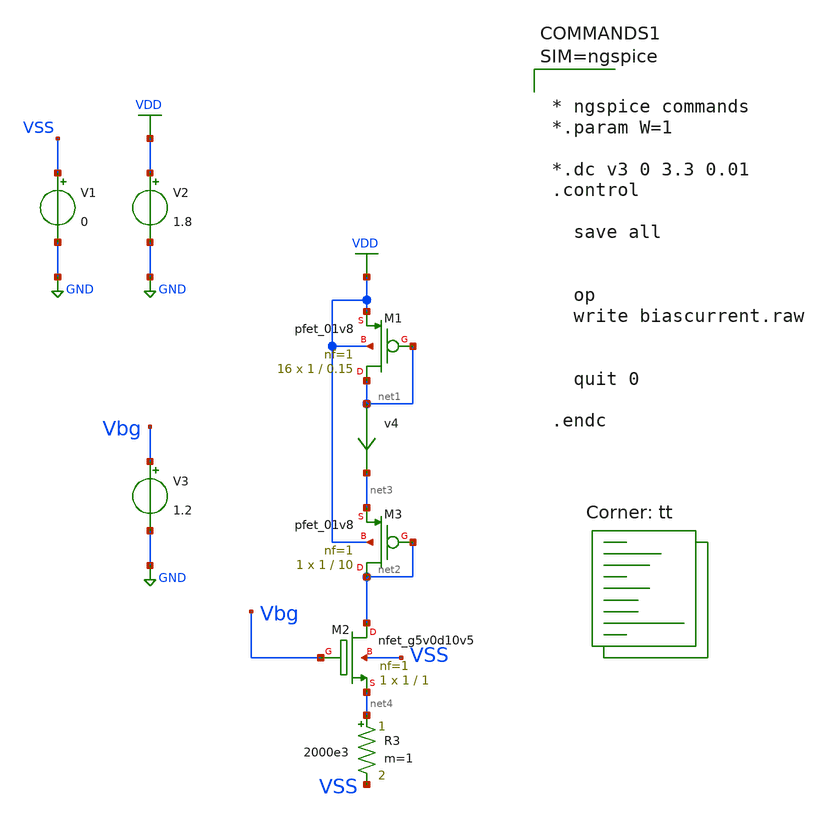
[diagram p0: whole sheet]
** sch_path: xschem/biascurrent.sch
**.subckt biascurrent
v4 net1 net3 0
.save i(v4)
V1 VSS GND 0
V2 VDD GND 1.8
XM1 net1 net1 VDD VDD sky130_fd_pr__pfet_01v8 L=0.15 W=1 nf=1 ad='int((nf+1)/2) * W/nf * 0.29' as='int((nf+2)/2) * W/nf * 0.29'
+ pd='2*int((nf+1)/2) * (W/nf + 0.29)' ps='2*int((nf+2)/2) * (W/nf + 0.29)' nrd='0.29 / W' nrs='0.29 / W'
+ sa=0 sb=0 sd=0 mult=16 m=16
V3 Vbg GND 1.2
XM2 net2 Vbg net4 VSS sky130_fd_pr__nfet_g5v0d10v5 L=1 W=1 nf=1 ad='int((nf+1)/2) * W/nf * 0.29' as='int((nf+2)/2) * W/nf * 0.29'
+ pd='2*int((nf+1)/2) * (W/nf + 0.29)' ps='2*int((nf+2)/2) * (W/nf + 0.29)' nrd='0.29 / W' nrs='0.29 / W'
+ sa=0 sb=0 sd=0 mult=1 m=1
XM3 net2 net2 net3 VDD sky130_fd_pr__pfet_01v8 L=10 W=1 nf=1 ad='int((nf+1)/2) * W/nf * 0.29' as='int((nf+2)/2) * W/nf * 0.29'
+ pd='2*int((nf+1)/2) * (W/nf + 0.29)' ps='2*int((nf+2)/2) * (W/nf + 0.29)' nrd='0.29 / W' nrs='0.29 / W'
+ sa=0 sb=0 sd=0 mult=1 m=1
R3 net4 VSS 2000e3 m=1
**** begin user architecture code



* ngspice commands
*.param W=1

*.dc v3 0 3.3 0.01
.control

  save all


  op
  write biascurrent.raw


  quit 0

.endc



.lib $::SKYWATER_MODELS/sky130.lib.spice tt
**** end user architecture code
**.ends
.GLOBAL GND
.GLOBAL VDD
.end
